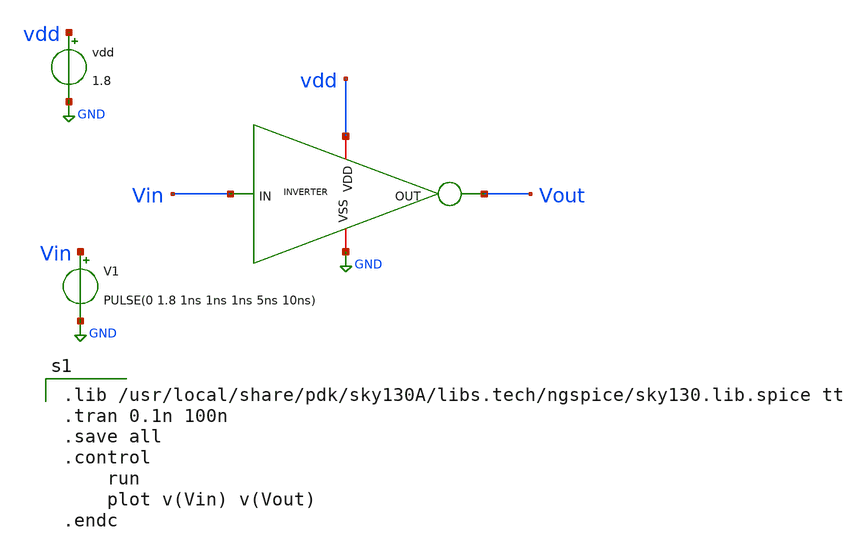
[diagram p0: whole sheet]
** sch_path: DECODER3TO8/Schematic/CMOS_INVERTER.sch
**.subckt CMOS_INVERTER
V1 Vin GND PULSE(0 1.8 1ns 1ns 1ns 5ns 10ns)
vdd vdd GND 1.8
x1 vdd Vin Vout GND INVERTER
**** begin user architecture code

.lib /usr/local/share/pdk/sky130A/libs.tech/ngspice/sky130.lib.spice tt
.tran 0.1n 100n
.save all
.control
	run
	plot v(Vin) v(Vout)
.endc

**** end user architecture code
**.ends

* expanding   symbol:  /home/nguyen2604/projects/DECODER3TO8/Schematic/INVERTER.sym # of pins=4
** sym_path: DECODER3TO8/Schematic/INVERTER.sym
** sch_path: DECODER3TO8/Schematic/INVERTER.sch
.subckt INVERTER VDD IN OUT VSS
*.ipin IN
*.opin OUT
*.iopin VDD
*.iopin VSS
XM2 OUT IN VDD VDD sky130_fd_pr__pfet_01v8 L=0.15 W=1 nf=1 ad='int((1 + 1)/2) * 1 / 1 * 0.29' as='int((1 + 2)/2) * 1 / 1 * 0.29'
+ pd='2*int((1 + 1)/2) * (1 / 1 + 0.29)' ps='2*int((1 + 2)/2) * (1 / 1 + 0.29)' nrd='0.29 / 1 ' nrs='0.29 / 1 '
+ sa=0 sb=0 sd=0 mult=1 m=1
XM1 OUT IN VSS VSS sky130_fd_pr__nfet_01v8 L=0.15 W=1 nf=1 ad='int((1 + 1)/2) * 1 / 1 * 0.29' as='int((1 + 2)/2) * 1 / 1 * 0.29'
+ pd='2*int((1 + 1)/2) * (1 / 1 + 0.29)' ps='2*int((1 + 2)/2) * (1 / 1 + 0.29)' nrd='0.29 / 1 ' nrs='0.29 / 1 '
+ sa=0 sb=0 sd=0 mult=1 m=1
.ends

.GLOBAL GND
.end
